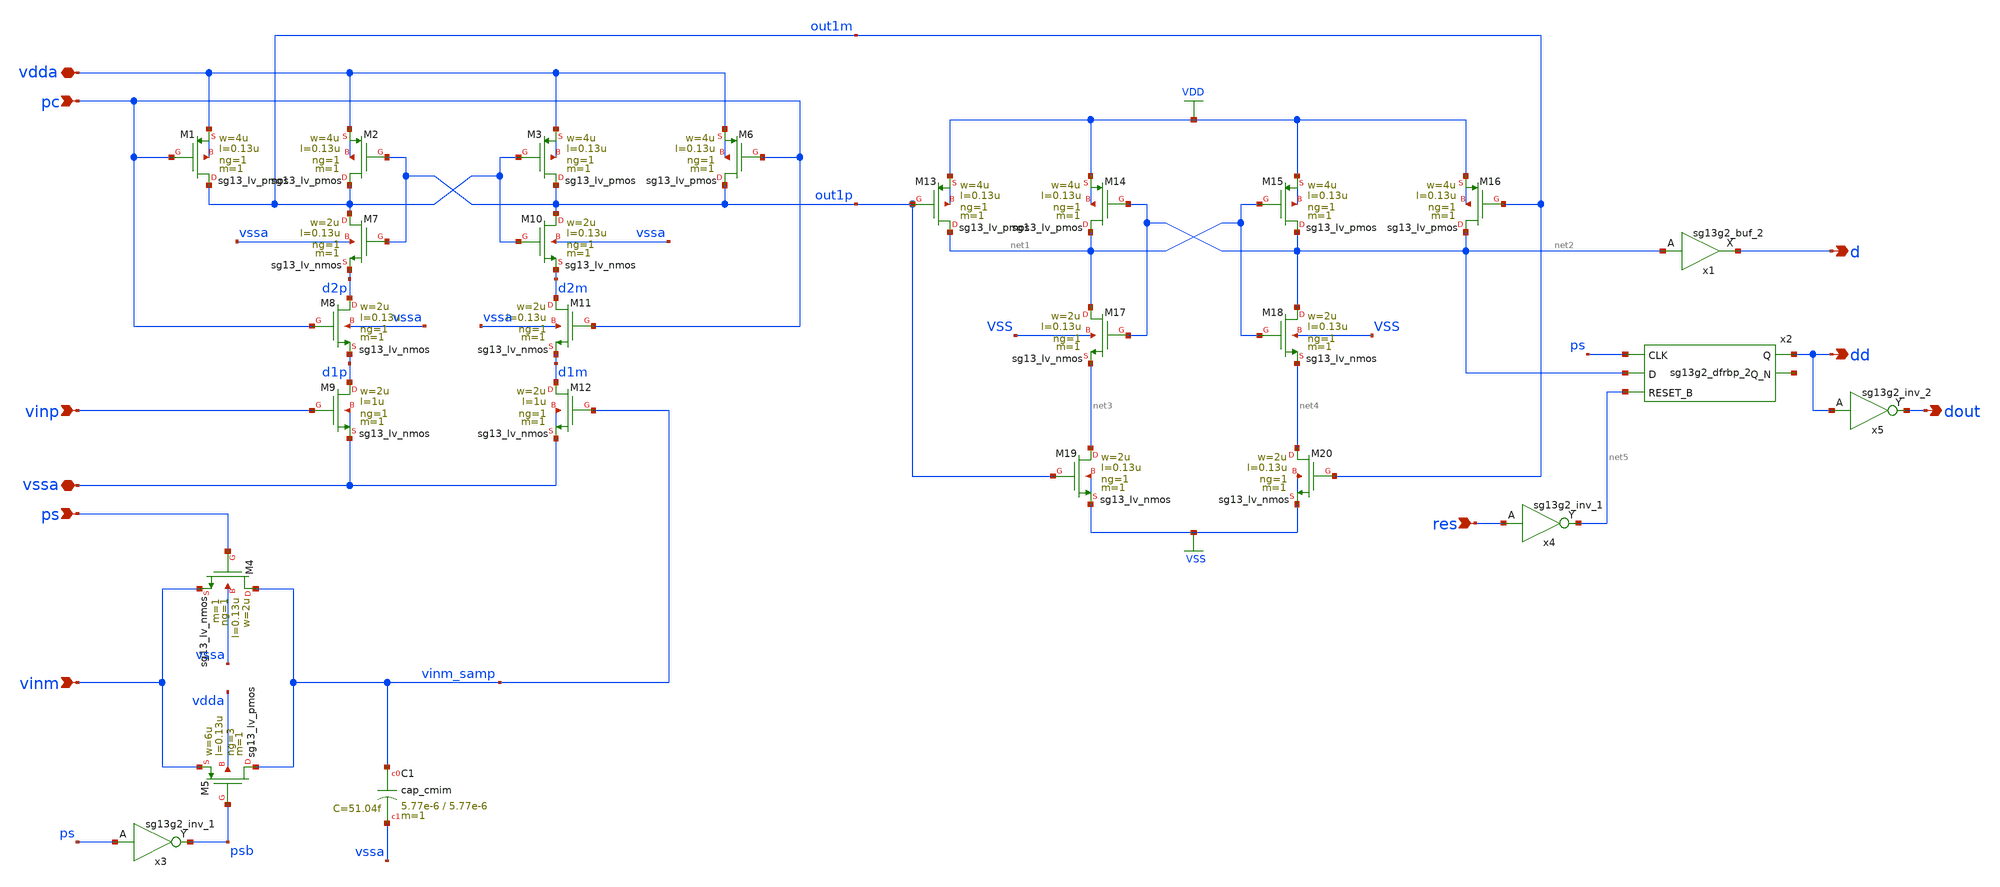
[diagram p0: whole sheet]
** sch_path: 5_Design/4_Layout/Team 1/xschem/comp_t1.sch
* IHP-GmbH/IHP-Open-PDK/ihp-sg13g2/libs.tech/xschem/sg13g2_stdcells/sg13g2_inv_2.sch:
* Copyright 2023 IHP PDK Authors
* Licensed under the Apache License, Version 2.0 (the "License");
**.subckt comp_t1 pc vinp ps vinm vdda vssa d dd res dout
*.ipin pc
*.ipin vinp
*.ipin ps
*.ipin vinm
*.iopin vdda
*.iopin vssa
*.opin d
*.opin dd
*.ipin res
*.opin dout
XM4 vinm_samp ps vinm vssa sg13_lv_nmos w=2u l=0.13u ng=1 m=1 mm_ok=1
XM5 vinm_samp psb vinm vdda sg13_lv_pmos w=6u l=0.13u ng=3 m=1 mm_ok=1
x3 psb ps VDD VSS sg13g2_inv_1
XC1 vinm_samp vssa cap_cmim w=5.77e-6 l=5.77e-6 m=1 mm_ok=1
XM1 out1m pc vdda vdda sg13_lv_pmos w=4u l=0.13u ng=1 m=1 mm_ok=1
XM2 out1m out1p vdda vdda sg13_lv_pmos w=4u l=0.13u ng=1 m=1 mm_ok=1
XM3 out1p out1m vdda vdda sg13_lv_pmos w=4u l=0.13u ng=1 m=1 mm_ok=1
XM6 out1p pc vdda vdda sg13_lv_pmos w=4u l=0.13u ng=1 m=1 mm_ok=1
XM7 out1m out1p d2p vssa sg13_lv_nmos w=2u l=0.13u ng=1 m=1 mm_ok=1
XM8 d2p pc d1p vssa sg13_lv_nmos w=2u l=0.13u ng=1 m=1 mm_ok=1
XM9 d1p vinp vssa vssa sg13_lv_nmos w=2u l=1u ng=1 m=1 mm_ok=1
XM10 out1p out1m d2m vssa sg13_lv_nmos w=2u l=0.13u ng=1 m=1 mm_ok=1
XM11 d2m pc d1m vssa sg13_lv_nmos w=2u l=0.13u ng=1 m=1 mm_ok=1
XM12 d1m vinm_samp vssa vssa sg13_lv_nmos w=2u l=1u ng=1 m=1 mm_ok=1
XM13 net1 out1p VDD VDD sg13_lv_pmos w=4u l=0.13u ng=1 m=1 mm_ok=1
XM14 net1 net2 VDD VDD sg13_lv_pmos w=4u l=0.13u ng=1 m=1 mm_ok=1
XM15 net2 net1 VDD VDD sg13_lv_pmos w=4u l=0.13u ng=1 m=1 mm_ok=1
XM16 net2 out1m VDD VDD sg13_lv_pmos w=4u l=0.13u ng=1 m=1 mm_ok=1
XM17 net1 net2 net3 VSS sg13_lv_nmos w=2u l=0.13u ng=1 m=1 mm_ok=1
XM18 net2 net1 net4 VSS sg13_lv_nmos w=2u l=0.13u ng=1 m=1 mm_ok=1
XM19 net3 out1p VSS VSS sg13_lv_nmos w=2u l=0.13u ng=1 m=1 mm_ok=1
XM20 net4 out1m VSS VSS sg13_lv_nmos w=2u l=0.13u ng=1 m=1 mm_ok=1
x1 d net2 VDD VSS sg13g2_buf_2
x2 dd net6 ps net2 net5 VDD VSS sg13g2_dfrbp_2
x4 net5 res VDD VSS sg13g2_inv_1
x5 dout dd VDD VSS sg13g2_inv_2
**.ends

* expanding   symbol:  sg13g2_stdcells/sg13g2_inv_1.sym # of pins=2
** sym_path: sg13g2_stdcells/sg13g2_inv_1.sym
** sch_path: sg13g2_stdcells/sg13g2_inv_1.sch
.subckt sg13g2_inv_1 Y A VDD VSS
*.opin Y
*.ipin A
*.iopin VDD
*.iopin VSS
XM1 Y A VSS VSS sg13_lv_nmos w=740.00n l=130.00n ng=1 m=1 mm_ok=1
XM2 Y A VDD VDD sg13_lv_pmos w=1.12u l=130.00n ng=1 m=1 mm_ok=1
.ends


* expanding   symbol:  sg13g2_stdcells/sg13g2_buf_2.sym # of pins=2
** sym_path: sg13g2_stdcells/sg13g2_buf_2.sym
** sch_path: sg13g2_stdcells/sg13g2_buf_2.sch
.subckt sg13g2_buf_2 X A VDD VSS
*.ipin A
*.opin X
*.iopin VDD
*.iopin VSS
XM1 net1 A VSS VSS sg13_lv_nmos w=640.00n l=130.00n ng=1 m=1 mm_ok=1
XM2 X net1 VSS VSS sg13_lv_nmos w=1.48u l=130.00n ng=2 m=1 mm_ok=1
XM3 net1 A VDD VDD sg13_lv_pmos w=1.000u l=130.00n ng=1 m=1 mm_ok=1
XM4 X net1 VDD VDD sg13_lv_pmos w=2.24u l=130.00n ng=2 m=1 mm_ok=1
.ends


* expanding   symbol:  sg13g2_stdcells/sg13g2_dfrbp_2.sym # of pins=5
** sym_path: sg13g2_stdcells/sg13g2_dfrbp_2.sym
** sch_path: sg13g2_stdcells/sg13g2_dfrbp_2.sch
.subckt sg13g2_dfrbp_2 Q Q_N CLK D RESET_B VDD VSS
*.ipin D
*.ipin RESET_B
*.ipin CLK
*.opin Q
*.opin Q_N
*.iopin VDD
*.iopin VSS
XM1 Db D net12 VSS sg13_lv_nmos w=420.00n l=130.00n ng=1 m=1 mm_ok=1
XM2 net12 RESET_B VSS VSS sg13_lv_nmos w=420.00n l=130.00n ng=1 m=1 mm_ok=1
XM3 net2 clkneg net11 VSS sg13_lv_nmos w=420.00n l=130.00n ng=1 m=1 mm_ok=1
XM4 net11 net3 VSS VSS sg13_lv_nmos w=420.00n l=130.00n ng=1 m=1 mm_ok=1
XM5 net3 net2 net7 VSS sg13_lv_nmos w=420.00n l=130.00n ng=1 m=1 mm_ok=1
XM6 net7 RESET_B VSS VSS sg13_lv_nmos w=420.00n l=130.00n ng=1 m=1 mm_ok=1
XM7 Q_N net2 VSS VSS sg13_lv_nmos w=1.48u l=130.00n ng=2 m=1 mm_ok=1
XM8 net1 net2 VSS VSS sg13_lv_nmos w=640.00n l=130.00n ng=1 m=1 mm_ok=1
XM9 Q net1 VSS VSS sg13_lv_nmos w=1.48u l=130.00n ng=2 m=1 mm_ok=1
XM10 clkneg CLK VSS VSS sg13_lv_nmos w=740.00n l=130.00n ng=1 m=1 mm_ok=1
XM11 clkpos clkneg VSS VSS sg13_lv_nmos w=740.00n l=130.00n ng=1 m=1 mm_ok=1
XM12 Db clkneg net4 VSS sg13_lv_nmos w=420.00n l=130.00n ng=1 m=1 mm_ok=1
XM13 net4 clkpos net10 VSS sg13_lv_nmos w=420.00n l=130.00n ng=1 m=1 mm_ok=1
XM14 net10 net5 net6 VSS sg13_lv_nmos w=420.00n l=130.00n ng=1 m=1 mm_ok=1
XM15 net6 RESET_B VSS VSS sg13_lv_nmos w=420.00n l=130.00n ng=1 m=1 mm_ok=1
XM16 net5 net4 VSS VSS sg13_lv_nmos w=740.00n l=130.00n ng=1 m=1 mm_ok=1
XM17 net5 clkpos net2 VSS sg13_lv_nmos w=740.00n l=130.00n ng=1 m=1 mm_ok=1
XM18 Db RESET_B VDD VDD sg13_lv_pmos w=420.00n l=130.00n ng=1 m=1 mm_ok=1
XM19 Db D VDD VDD sg13_lv_pmos w=420.00n l=130.00n ng=1 m=1 mm_ok=1
XM20 net9 net3 VDD VDD sg13_lv_pmos w=420.00n l=130.00n ng=1 m=1 mm_ok=1
XM21 net2 clkpos net9 VDD sg13_lv_pmos w=420.00n l=130.00n ng=1 m=1 mm_ok=1
XM22 net3 net2 VDD VDD sg13_lv_pmos w=420.00n l=130.00n ng=1 m=1 mm_ok=1
XM23 net3 RESET_B VDD VDD sg13_lv_pmos w=420.00n l=130.00n ng=1 m=1 mm_ok=1
XM24 Q_N net2 VDD VDD sg13_lv_pmos w=2.24u l=130.00n ng=2 m=1 mm_ok=1
XM25 net1 net2 VDD VDD sg13_lv_pmos w=1.000u l=130.00n ng=1 m=1 mm_ok=1
XM26 Q net1 VDD VDD sg13_lv_pmos w=2.24u l=130.00n ng=2 m=1 mm_ok=1
XM27 clkneg CLK VDD VDD sg13_lv_pmos w=1.12u l=130.00n ng=1 m=1 mm_ok=1
XM28 clkpos clkneg VDD VDD sg13_lv_pmos w=1.12u l=130.00n ng=1 m=1 mm_ok=1
XM29 Db clkpos net4 VDD sg13_lv_pmos w=420.00n l=130.00n ng=1 m=1 mm_ok=1
XM30 net8 net5 VDD VDD sg13_lv_pmos w=420.00n l=130.00n ng=1 m=1 mm_ok=1
XM31 net4 clkneg net8 VDD sg13_lv_pmos w=420.00n l=130.00n ng=1 m=1 mm_ok=1
XM32 net4 RESET_B VDD VDD sg13_lv_pmos w=420.00n l=130.00n ng=1 m=1 mm_ok=1
XM33 net5 net4 VDD VDD sg13_lv_pmos w=1.000u l=130.00n ng=1 m=1 mm_ok=1
XM34 net5 clkneg net2 VDD sg13_lv_pmos w=1.000u l=130.00n ng=1 m=1 mm_ok=1
.ends


* expanding   symbol:  sg13g2_stdcells/sg13g2_inv_2.sym # of pins=2
** sym_path: sg13g2_stdcells/sg13g2_inv_2.sym
** sch_path: sg13g2_stdcells/sg13g2_inv_2.sch
.subckt sg13g2_inv_2 Y A VDD VSS
*.opin Y
*.ipin A
*.iopin VDD
*.iopin VSS
XM1 Y A VSS VSS sg13_lv_nmos w=1.48u l=130.00n ng=2 m=1 mm_ok=1
XM2 Y A VDD VDD sg13_lv_pmos w=2.24u l=130.00n ng=2 m=1 mm_ok=1
.ends

.GLOBAL VDD
.GLOBAL VSS
.end
